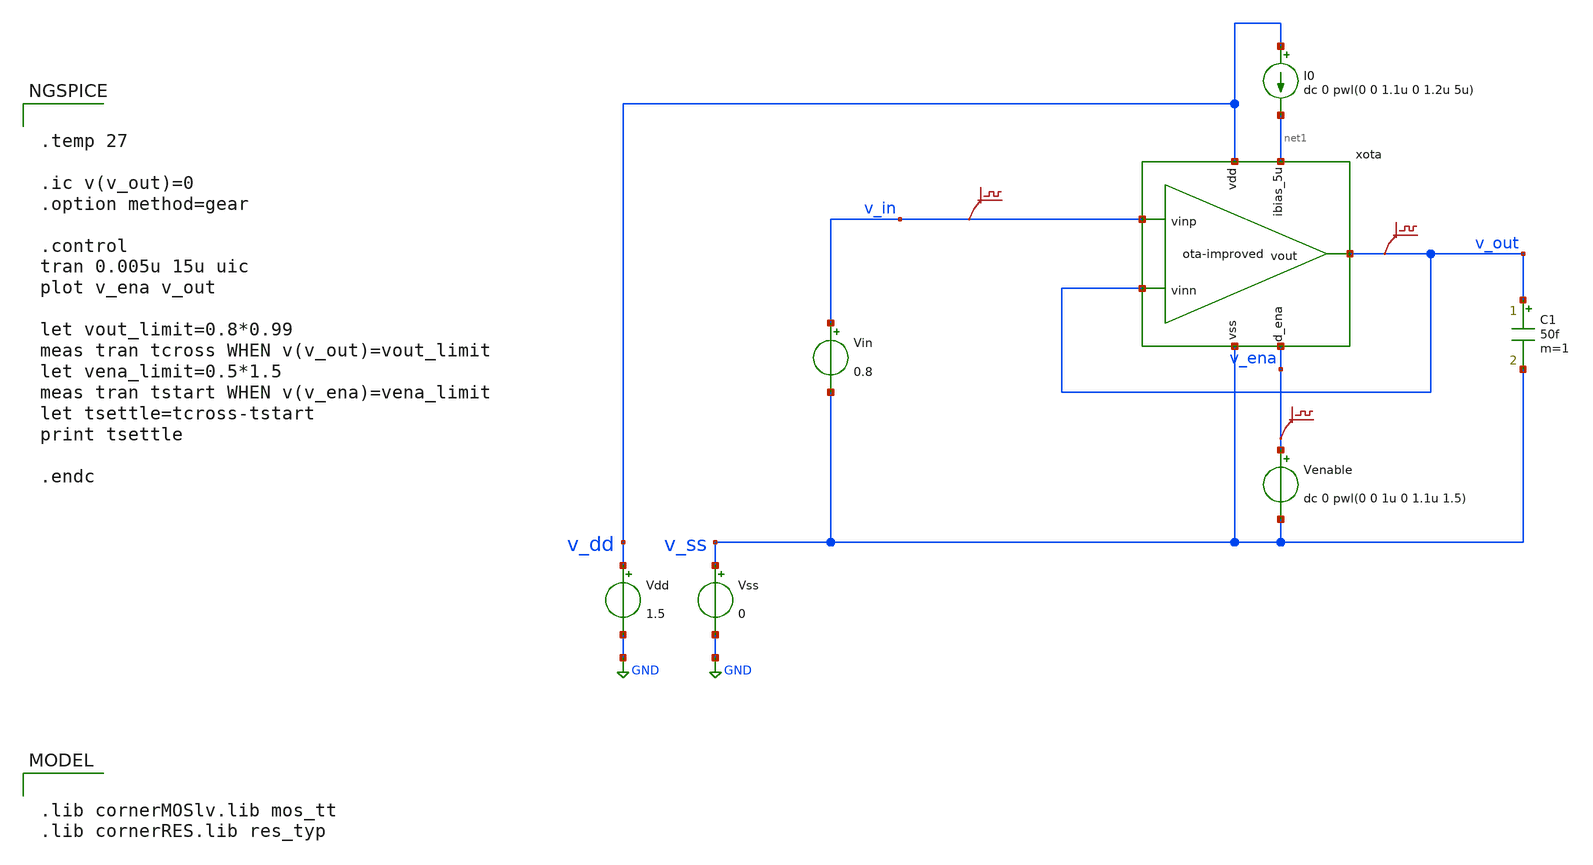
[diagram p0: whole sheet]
** sch_path: xschem/ota-improved_tb-tran.sch
* (c) 2024-2025 H. Pretl, Apache-2.0 license
**.subckt ota-improved_tb-tran
Vdd v_dd GND 1.5
xota v_dd v_out v_in v_out net1 v_ena v_ss ota-improved
Vss v_ss GND 0
C1 v_out v_ss 50f m=1
Vin v_in v_ss 0.8
I0 v_dd net1 dc 0 pwl(0 0 1.1u 0 1.2u 5u)
Venable v_ena v_ss dc 0 pwl(0 0 1u 0 1.1u 1.5)
.save v(v_in)
.save v(v_out)
.save v(v_ena)
**** begin user architecture code


.temp 27

.ic v(v_out)=0
.option method=gear

.control
tran 0.005u 15u uic
plot v_ena v_out

let vout_limit=0.8*0.99
meas tran tcross WHEN v(v_out)=vout_limit
let vena_limit=0.5*1.5
meas tran tstart WHEN v(v_ena)=vena_limit
let tsettle=tcross-tstart
print tsettle

.endc



.lib cornerMOSlv.lib mos_tt
.lib cornerRES.lib res_typ

**** end user architecture code
**.ends
.GLOBAL GND
.end
